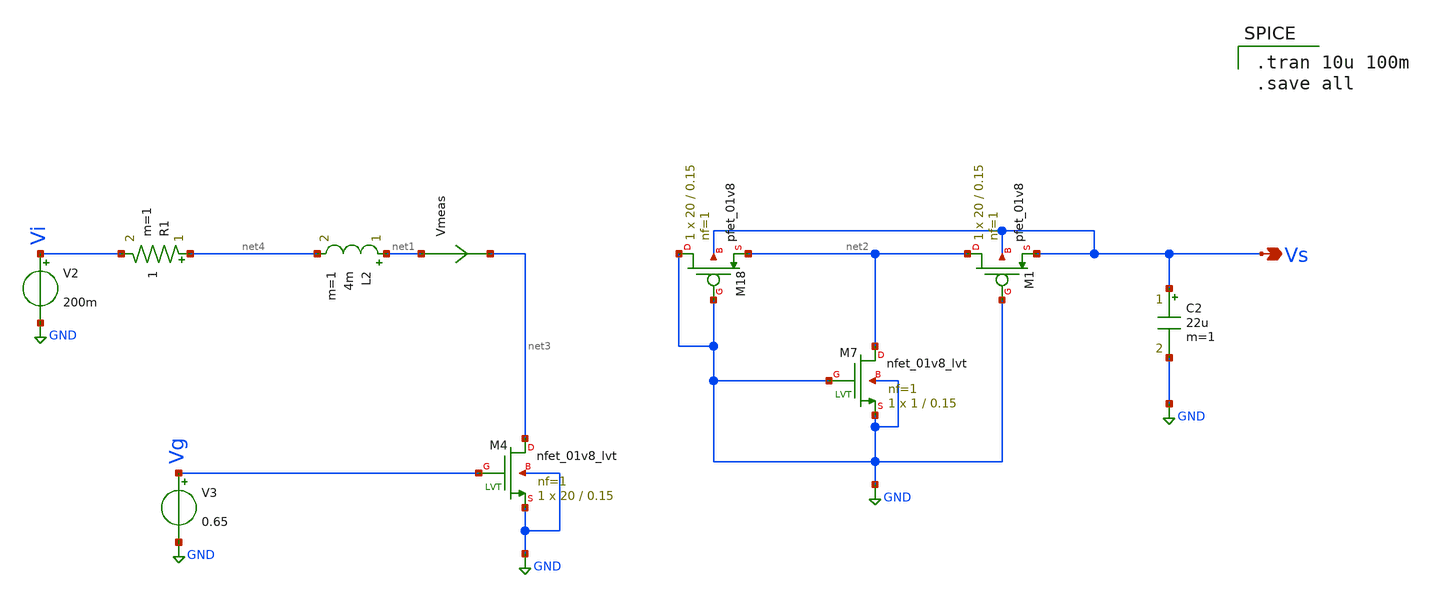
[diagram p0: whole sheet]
** sch_path: Blocks/Startup Converter/Boost_Conv1.sch
**.subckt Boost_Conv1 Vs
*.opin Vs
L2 net1 net4 4m m=1
C2 Vs GND 22u m=1
XM4 net3 Vg GND GND sky130_fd_pr__nfet_01v8_lvt L=0.15 W=20 nf=1 ad='int((nf+1)/2) * W/nf * 0.29' as='int((nf+2)/2) * W/nf * 0.29'
+ pd='2*int((nf+1)/2) * (W/nf + 0.29)' ps='2*int((nf+2)/2) * (W/nf + 0.29)' nrd='0.29 / W' nrs='0.29 / W'
+ sa=0 sb=0 sd=0 mult=1 m=1
XM7 net2 GND GND GND sky130_fd_pr__nfet_01v8_lvt L=0.15 W=1 nf=1 ad='int((nf+1)/2) * W/nf * 0.29' as='int((nf+2)/2) * W/nf * 0.29'
+ pd='2*int((nf+1)/2) * (W/nf + 0.29)' ps='2*int((nf+2)/2) * (W/nf + 0.29)' nrd='0.29 / W' nrs='0.29 / W'
+ sa=0 sb=0 sd=0 mult=1 m=1
V2 Vi GND 200m
XM18 GND GND net2 Vs sky130_fd_pr__pfet_01v8 L=0.15 W=20 nf=1 ad='int((nf+1)/2) * W/nf * 0.29' as='int((nf+2)/2) * W/nf * 0.29'
+ pd='2*int((nf+1)/2) * (W/nf + 0.29)' ps='2*int((nf+2)/2) * (W/nf + 0.29)' nrd='0.29 / W' nrs='0.29 / W'
+ sa=0 sb=0 sd=0 mult=1 m=1
XM1 net2 GND Vs Vs sky130_fd_pr__pfet_01v8 L=0.15 W=20 nf=1 ad='int((nf+1)/2) * W/nf * 0.29' as='int((nf+2)/2) * W/nf * 0.29'
+ pd='2*int((nf+1)/2) * (W/nf + 0.29)' ps='2*int((nf+2)/2) * (W/nf + 0.29)' nrd='0.29 / W' nrs='0.29 / W'
+ sa=0 sb=0 sd=0 mult=1 m=1
V3 Vg GND 0.65
Vmeas net1 net3 0
.save i(vmeas)
R1 net4 Vi 1 m=1
**** begin user architecture code

** opencircuitdesign pdks install
.lib $::SKYWATER_MODELS/sky130.lib.spice tt



.tran 10u 100m
.save all

**** end user architecture code
**.ends
.GLOBAL GND
.end
